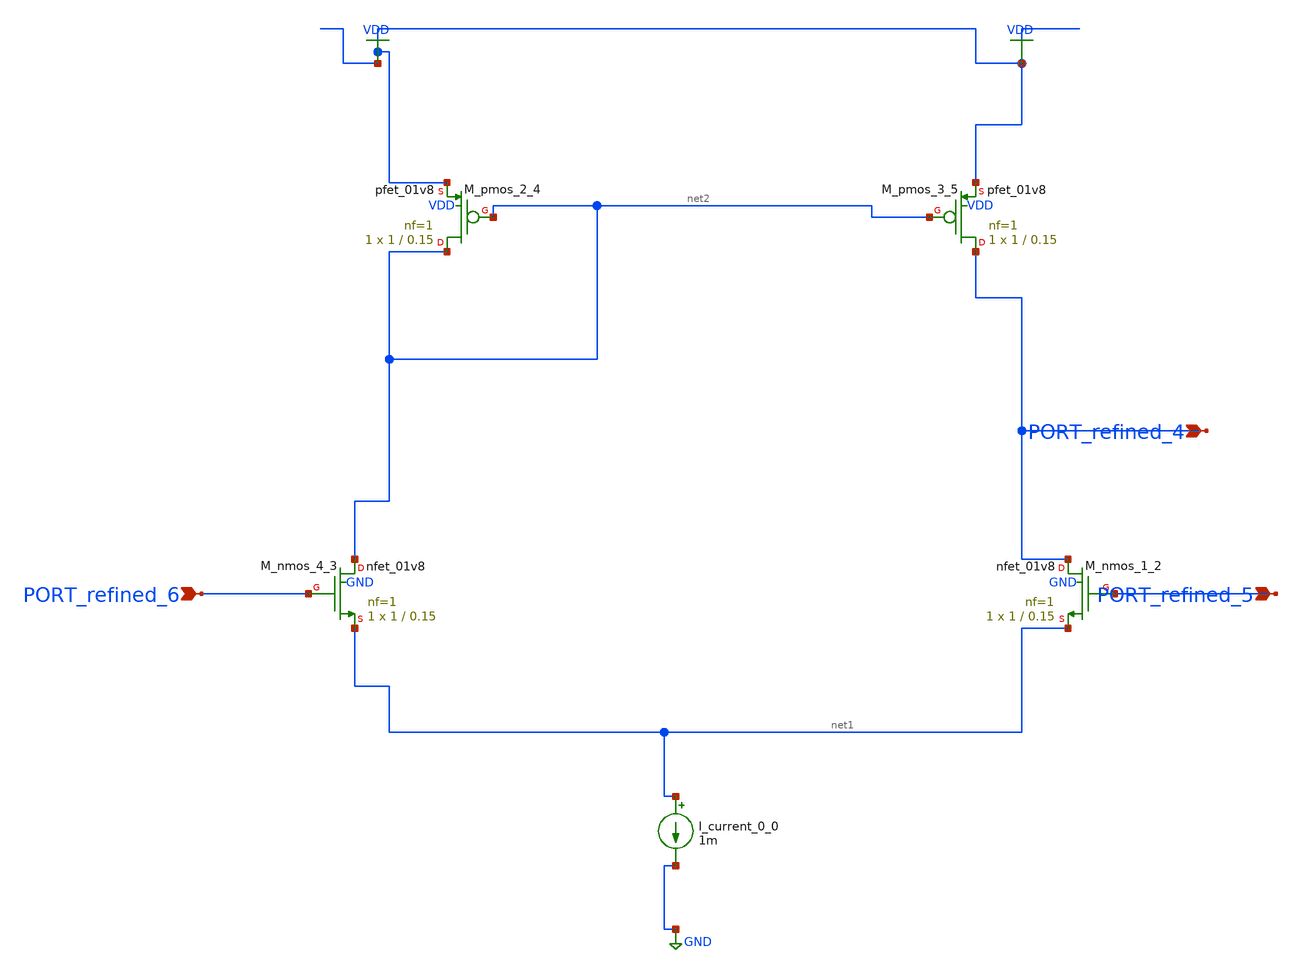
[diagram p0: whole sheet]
** sch_path: schematics/AMSNet/275.sch
**.subckt 275 PORT_refined_6 PORT_refined_5 PORT_refined_4
*.ipin PORT_refined_6
*.ipin PORT_refined_5
*.ipin PORT_refined_4
I_current_0_0 net1 GND 1m
XM_nmos_1_2 PORT_refined_4 PORT_refined_5 net1 GND sky130_fd_pr__nfet_01v8 L=0.15 W=1 nf=1 ad='int((1 + 1)/2) * 1 / 1 * 0.29'
+ as='int((1 + 2)/2) * 1 / 1 * 0.29' pd='2*int((1 + 1)/2) * (1 / 1 + 0.29)' ps='2*int((1 + 2)/2) * (1 / 1 + 0.29)'
+ nrd='0.29 / 1 ' nrs='0.29 / 1 ' sa=0 sb=0 sd=0 mult=1 m=1
XM_nmos_4_3 net2 PORT_refined_6 net1 GND sky130_fd_pr__nfet_01v8 L=0.15 W=1 nf=1 ad='int((1 + 1)/2) * 1 / 1 * 0.29'
+ as='int((1 + 2)/2) * 1 / 1 * 0.29' pd='2*int((1 + 1)/2) * (1 / 1 + 0.29)' ps='2*int((1 + 2)/2) * (1 / 1 + 0.29)'
+ nrd='0.29 / 1 ' nrs='0.29 / 1 ' sa=0 sb=0 sd=0 mult=1 m=1
XM_pmos_2_4 net2 net2 VDD VDD sky130_fd_pr__pfet_01v8 L=0.15 W=1 nf=1 ad='int((1 + 1)/2) * 1 / 1 * 0.29'
+ as='int((1 + 2)/2) * 1 / 1 * 0.29' pd='2*int((1 + 1)/2) * (1 / 1 + 0.29)' ps='2*int((1 + 2)/2) * (1 / 1 + 0.29)'
+ nrd='0.29 / 1 ' nrs='0.29 / 1 ' sa=0 sb=0 sd=0 mult=1 m=1
XM_pmos_3_5 PORT_refined_4 net2 VDD VDD sky130_fd_pr__pfet_01v8 L=0.15 W=1 nf=1 ad='int((1 + 1)/2) * 1 / 1 * 0.29'
+ as='int((1 + 2)/2) * 1 / 1 * 0.29' pd='2*int((1 + 1)/2) * (1 / 1 + 0.29)' ps='2*int((1 + 2)/2) * (1 / 1 + 0.29)'
+ nrd='0.29 / 1 ' nrs='0.29 / 1 ' sa=0 sb=0 sd=0 mult=1 m=1
**.ends
.GLOBAL GND
.GLOBAL VDD
.end
